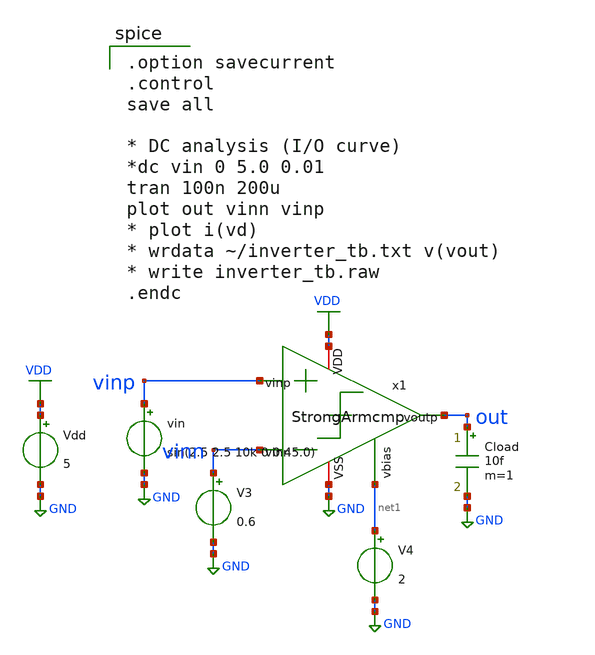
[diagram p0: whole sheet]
** sch_path: IO_202604/08/xschem/StrongArmcmp_sim.sch
**.subckt StrongArmcmp_sim
Vdd VDD GND 5
vin vinp GND sin(2.5 2.5 10k 0 0 45.0)
V3 vinn GND 0.6
V4 net1 GND 2
Cload out GND 10f m=1
x1 VDD vinn vinp out net1 GND StrongArmcmp
**** begin user architecture code
 .include $::LIB/../ip62_models

.option savecurrent
.control
save all

* DC analysis (I/O curve)
*dc vin 0 5.0 0.01
tran 100n 200u
plot out vinn vinp
* plot i(vd)
* wrdata ~/inverter_tb.txt v(vout)
* write inverter_tb.raw
.endc

**** end user architecture code
**.ends
.GLOBAL GND
.GLOBAL VDD
.end
